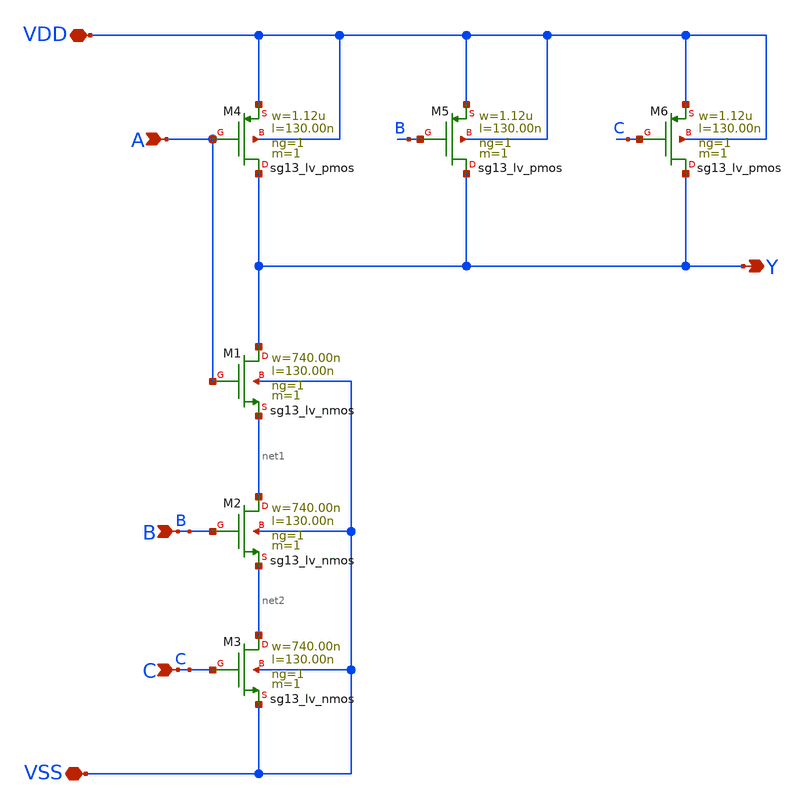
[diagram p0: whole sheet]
** sch_path: ihp-sg13g2/libs.tech/xschem/sg13g2_stdcells/sg13g2_nand3_1.sch
**.subckt sg13g2_nand3_1 A B C Y VDD VSS
*.ipin A
*.ipin B
*.ipin C
*.opin Y
*.iopin VDD
*.iopin VSS
XM1 Y A net1 VSS sg13_lv_nmos w=740.00n l=130.00n ng=1 m=1 mm_ok=1
XM2 net1 B net2 VSS sg13_lv_nmos w=740.00n l=130.00n ng=1 m=1 mm_ok=1
XM3 net2 C VSS VSS sg13_lv_nmos w=740.00n l=130.00n ng=1 m=1 mm_ok=1
XM4 Y A VDD VDD sg13_lv_pmos w=1.12u l=130.00n ng=1 m=1 mm_ok=1
XM5 Y B VDD VDD sg13_lv_pmos w=1.12u l=130.00n ng=1 m=1 mm_ok=1
XM6 Y C VDD VDD sg13_lv_pmos w=1.12u l=130.00n ng=1 m=1 mm_ok=1
**.ends
.end
